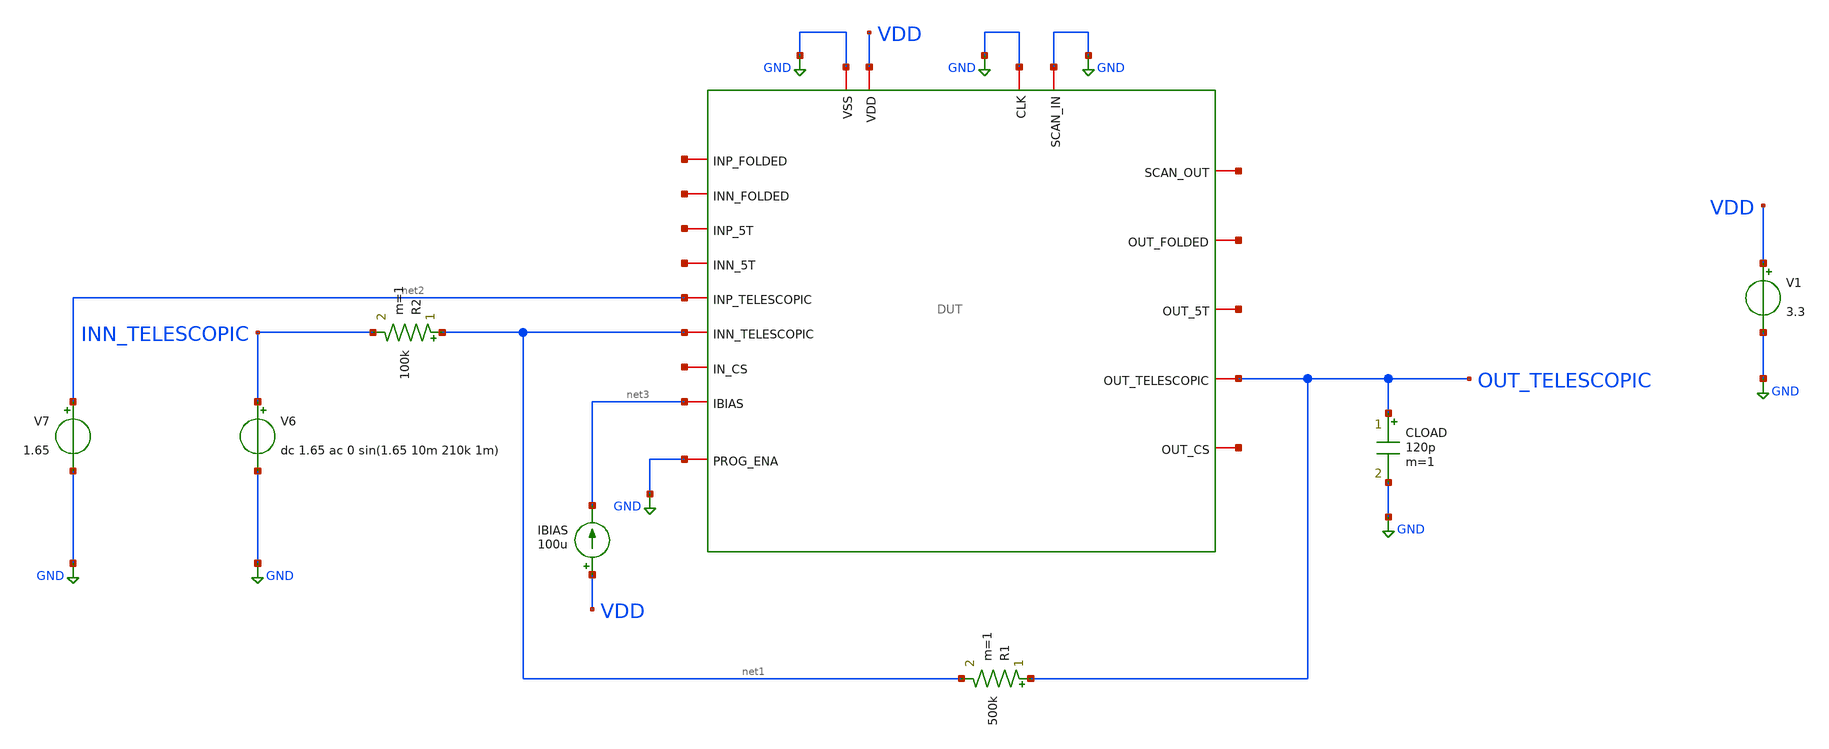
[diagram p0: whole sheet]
** sch_path: designs/libs/verification/ota_telescopic/default/bw.sch
**.subckt bw
x1 GND net4 GND GND VDD net5 net6 net7 net3 net8 net9 net10 net2 OUT_TELESCOPIC net11 net12 net1 GND
+ DUT
V1 VDD GND 3.3
CLOAD OUT_TELESCOPIC GND 120p m=1
R1 OUT_TELESCOPIC net1 500k m=1
R2 net1 INN_TELESCOPIC 100k m=1
V6 INN_TELESCOPIC GND dc 1.65 ac 0 sin(1.65 10m 210k 1m)
V7 net2 GND 1.65
IBIAS VDD net3 100u
**** begin user architecture code

.include $::180MCU_MODELS/design.ngspice
.lib $::180MCU_MODELS/sm141064.ngspice typical



.control
tran 1u 5m

meas tran vout_pp pp v(out_telescopic) from=2m to=5m
meas tran vin_pp pp v(inn_telescopic) from=2m to=5m
let gain = vout_pp / vin_pp
let gain_db = 20 * log(gain) / log(10)
print gain gain_db
.endc


**** end user architecture code
**.ends
.GLOBAL GND
.end
